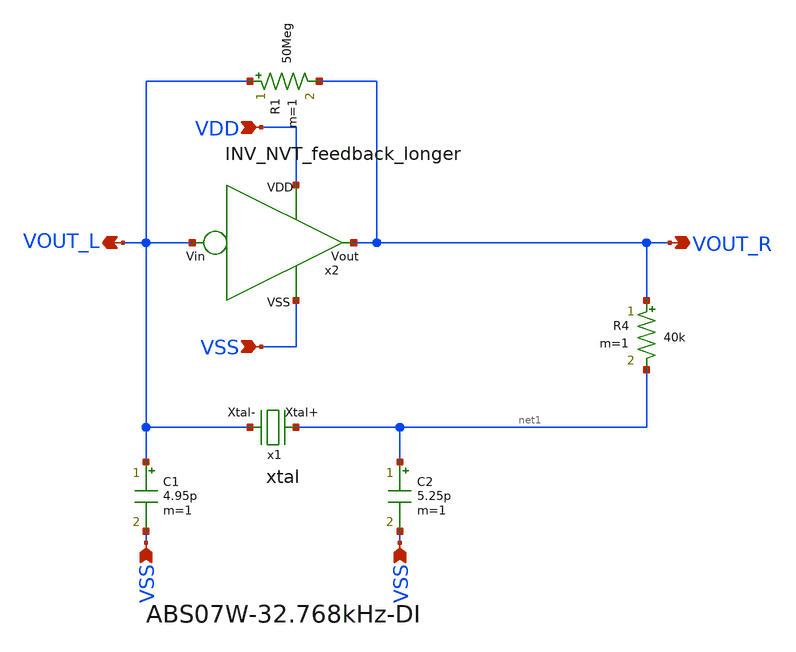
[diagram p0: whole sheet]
** sch_path: design/THESIS_EXP_RO_INVERTER_SKY130A/xtal_osc_NVT_LL.sch
**.subckt xtal_osc_NVT_LL VSS VSS VOUT_R VOUT_L VDD VSS
*.ipin VSS
*.ipin VSS
*.opin VOUT_R
*.opin VOUT_L
*.ipin VDD
*.ipin VSS
x1 net1 VOUT_L xtal
C1 VOUT_L VSS 4.95p m=1
C2 net1 VSS 5.25p m=1
R1 VOUT_L VOUT_R 50Meg m=1
R4 VOUT_R net1 40k m=1
x2 VDD VSS VOUT_R VOUT_L INV_NVT_feedback_longer
**.ends
.end
